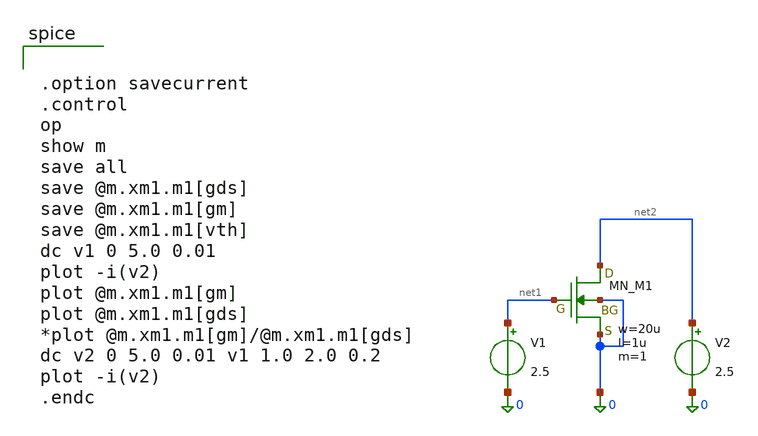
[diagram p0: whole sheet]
** sch_path: member_project/JJY_Receiver/Masahiro/jjy_recv/check_fet/nfet_gm.sch
**.subckt nfet_gm
XM1 net2 net1 0 0 NMOS w=20u l=1u as=0 ad=0 ps=0 pd=0 nrd=0 nrs=0 m=1
V1 net1 0 2.5
V2 net2 0 2.5
**** begin user architecture code
 .include $::LIB/ip62_models


.option savecurrent
.control
op
show m
save all
save @m.xm1.m1[gds]
save @m.xm1.m1[gm]
save @m.xm1.m1[vth]
dc v1 0 5.0 0.01
plot -i(v2)
plot @m.xm1.m1[gm]
plot @m.xm1.m1[gds]
*plot @m.xm1.m1[gm]/@m.xm1.m1[gds]
dc v2 0 5.0 0.01 v1 1.0 2.0 0.2
plot -i(v2)
.endc


**** end user architecture code
**.ends
.end
